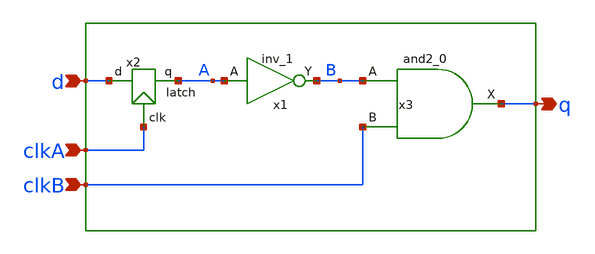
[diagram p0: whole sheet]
** sch_path: src/xe/test_cases/latch_and.sch
**.subckt latch_and d clkA q clkB
*.ipin d
*.ipin clkA
*.opin q
*.ipin clkB
x1 A vss vss vcc vcc B sky130_fd_sc_hd__inv_1
x3 B clkB vss vss vcc vcc q sky130_fd_sc_hd__and2_0
x2 clkA A d latch
**.ends

* expanding   symbol:  yxt/latch.sym # of pins=3
** sym_path: src/xe/test_cases/latch.sym
** sch_path: src/xe/test_cases/latch.sch
.subckt latch clk q d  vcc=vcc vss=vss
*.ipin clk
*.ipin d
*.opin q
x1 d vss vss vcc vcc db sky130_fd_sc_hd__inv_1
x2 clkb db z clk vcc vss tgate
x3 z vss vss vcc vcc q sky130_fd_sc_hd__inv_1
x6 clk vss vss vcc vcc clkb sky130_fd_sc_hd__inv_1
x4 z vss vss vcc vcc fb sky130_fd_sc_hd__inv_1
x5 fb vss vss vcc vcc z sky130_fd_sc_hd__inv_1
.ends


* expanding   symbol:  yxt/tgate.sym # of pins=4
** sym_path: src/xe/test_cases/tgate.sym
** sch_path: src/xe/test_cases/tgate.sch
.subckt tgate gp s d gn vcc vss
*.ipin s
*.ipin gp
*.ipin gn
*.opin d
XMpc d gp s vss sky130_fd_pr__pfet_01v8 L=0.15 W=1 nf=1 ad='int((nf+1)/2) * W/nf * 0.29' as='int((nf+2)/2) * W/nf * 0.29'
+ pd='2*int((nf+1)/2) * (W/nf + 0.29)' ps='2*int((nf+2)/2) * (W/nf + 0.29)' nrd='0.29 / W' nrs='0.29 / W'
+ sa=0 sb=0 sd=0 mult=7 m=7
XM15 s gn d vcc sky130_fd_pr__nfet_01v8 L=0.15 W=1 nf=1 ad='int((nf+1)/2) * W/nf * 0.29' as='int((nf+2)/2) * W/nf * 0.29'
+ pd='2*int((nf+1)/2) * (W/nf + 0.29)' ps='2*int((nf+2)/2) * (W/nf + 0.29)' nrd='0.29 / W' nrs='0.29 / W'
+ sa=0 sb=0 sd=0 mult=1 m=1
.ends

.end
